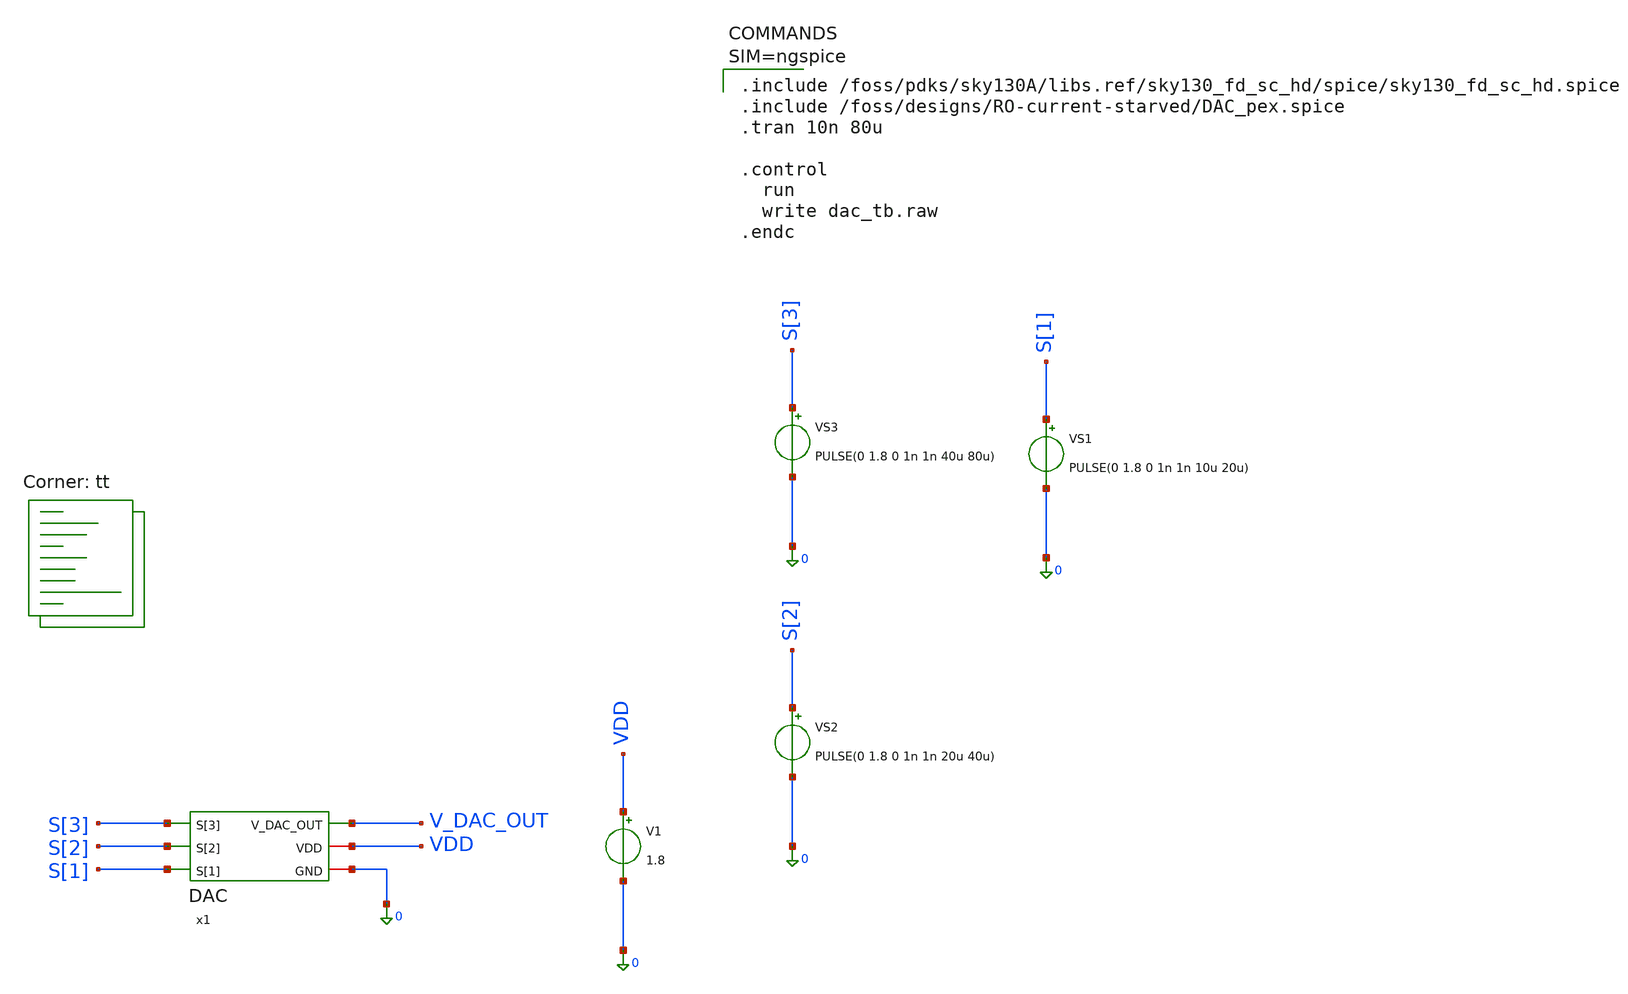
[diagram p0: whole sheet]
** sch_path: src/analog_source_files/DAC_tb.sch
**.subckt DAC_tb
x1 S[3] S[1] S[2] V_DAC_OUT VDD 0 DAC
V1 VDD 0 1.8
VS1 S[1] 0 PULSE(0 1.8 0 1n 1n 10u 20u)
VS2 S[2] 0 PULSE(0 1.8 0 1n 1n 20u 40u)
VS3 S[3] 0 PULSE(0 1.8 0 1n 1n 40u 80u)
**** begin user architecture code
.lib $::SKYWATER_MODELS/sky130.lib.spice tt


.include /foss/pdks/sky130A/libs.ref/sky130_fd_sc_hd/spice/sky130_fd_sc_hd.spice
.include /foss/designs/RO-current-starved/DAC_pex.spice
.tran 10n 80u

.control
  run
  write dac_tb.raw
.endc



**** end user architecture code
**.ends
.end
